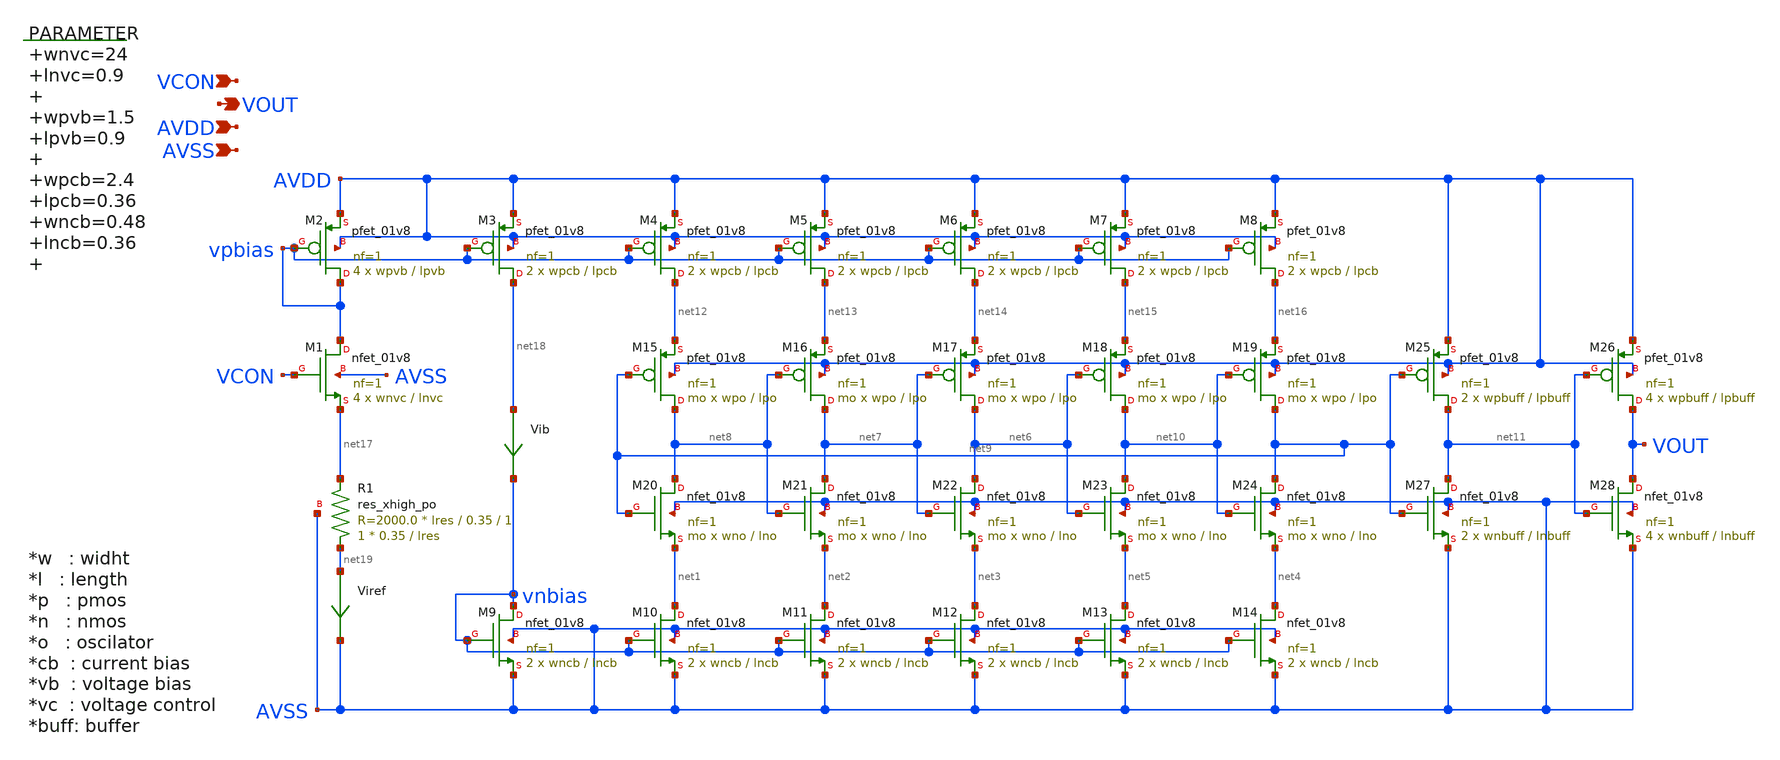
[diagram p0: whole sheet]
** sch_path: xschem/vco.sch
**.subckt vco VCON VOUT AVDD AVSS
*.ipin VCON
*.opin VOUT
*.ipin AVDD
*.ipin AVSS
.param wnvc=24 lnvc=0.9 wpvb=1.5 lpvb=0.9 wpcb=2.4 lpcb=0.36 wncb=0.48 lncb=0.36 wpo=2 lpo=0.54
+ wno=1 lno=0.54 mo=2 wpbuff=2.4 lpbuff=0.18 wnbuff=0.6 lnbuff=0.18 lres=5.25

XR1 net19 net17 AVSS sky130_fd_pr__res_xhigh_po W=0.35 L=lres mult=1 m=1
XM1 vpbias VCON net17 AVSS sky130_fd_pr__nfet_01v8 L=lnvc W=wnvc nf=1 ad='int((nf+1)/2) * W/nf * 0.29'
+ as='int((nf+2)/2) * W/nf * 0.29' pd='2*int((nf+1)/2) * (W/nf + 0.29)' ps='2*int((nf+2)/2) * (W/nf + 0.29)'
+ nrd='0.29 / W' nrs='0.29 / W' sa=0 sb=0 sd=0 mult=4 m=4
XM2 vpbias vpbias AVDD AVDD sky130_fd_pr__pfet_01v8 L=lpvb W=wpvb nf=1 ad='int((nf+1)/2) * W/nf * 0.29'
+ as='int((nf+2)/2) * W/nf * 0.29' pd='2*int((nf+1)/2) * (W/nf + 0.29)' ps='2*int((nf+2)/2) * (W/nf + 0.29)'
+ nrd='0.29 / W' nrs='0.29 / W' sa=0 sb=0 sd=0 mult=4 m=4
XM3 net18 vpbias AVDD AVDD sky130_fd_pr__pfet_01v8 L=lpcb W=wpcb nf=1 ad='int((nf+1)/2) * W/nf * 0.29'
+ as='int((nf+2)/2) * W/nf * 0.29' pd='2*int((nf+1)/2) * (W/nf + 0.29)' ps='2*int((nf+2)/2) * (W/nf + 0.29)'
+ nrd='0.29 / W' nrs='0.29 / W' sa=0 sb=0 sd=0 mult=2 m=2
XM4 net12 vpbias AVDD AVDD sky130_fd_pr__pfet_01v8 L=lpcb W=wpcb nf=1 ad='int((nf+1)/2) * W/nf * 0.29'
+ as='int((nf+2)/2) * W/nf * 0.29' pd='2*int((nf+1)/2) * (W/nf + 0.29)' ps='2*int((nf+2)/2) * (W/nf + 0.29)'
+ nrd='0.29 / W' nrs='0.29 / W' sa=0 sb=0 sd=0 mult=2 m=2
XM5 net13 vpbias AVDD AVDD sky130_fd_pr__pfet_01v8 L=lpcb W=wpcb nf=1 ad='int((nf+1)/2) * W/nf * 0.29'
+ as='int((nf+2)/2) * W/nf * 0.29' pd='2*int((nf+1)/2) * (W/nf + 0.29)' ps='2*int((nf+2)/2) * (W/nf + 0.29)'
+ nrd='0.29 / W' nrs='0.29 / W' sa=0 sb=0 sd=0 mult=2 m=2
XM6 net14 vpbias AVDD AVDD sky130_fd_pr__pfet_01v8 L=lpcb W=wpcb nf=1 ad='int((nf+1)/2) * W/nf * 0.29'
+ as='int((nf+2)/2) * W/nf * 0.29' pd='2*int((nf+1)/2) * (W/nf + 0.29)' ps='2*int((nf+2)/2) * (W/nf + 0.29)'
+ nrd='0.29 / W' nrs='0.29 / W' sa=0 sb=0 sd=0 mult=2 m=2
XM7 net15 vpbias AVDD AVDD sky130_fd_pr__pfet_01v8 L=lpcb W=wpcb nf=1 ad='int((nf+1)/2) * W/nf * 0.29'
+ as='int((nf+2)/2) * W/nf * 0.29' pd='2*int((nf+1)/2) * (W/nf + 0.29)' ps='2*int((nf+2)/2) * (W/nf + 0.29)'
+ nrd='0.29 / W' nrs='0.29 / W' sa=0 sb=0 sd=0 mult=2 m=2
XM8 net16 vpbias AVDD AVDD sky130_fd_pr__pfet_01v8 L=lpcb W=wpcb nf=1 ad='int((nf+1)/2) * W/nf * 0.29'
+ as='int((nf+2)/2) * W/nf * 0.29' pd='2*int((nf+1)/2) * (W/nf + 0.29)' ps='2*int((nf+2)/2) * (W/nf + 0.29)'
+ nrd='0.29 / W' nrs='0.29 / W' sa=0 sb=0 sd=0 mult=2 m=2
XM9 vnbias vnbias AVSS AVSS sky130_fd_pr__nfet_01v8 L=lncb W=wncb nf=1 ad='int((nf+1)/2) * W/nf * 0.29'
+ as='int((nf+2)/2) * W/nf * 0.29' pd='2*int((nf+1)/2) * (W/nf + 0.29)' ps='2*int((nf+2)/2) * (W/nf + 0.29)'
+ nrd='0.29 / W' nrs='0.29 / W' sa=0 sb=0 sd=0 mult=2 m=2
XM10 net1 vnbias AVSS AVSS sky130_fd_pr__nfet_01v8 L=lncb W=wncb nf=1 ad='int((nf+1)/2) * W/nf * 0.29'
+ as='int((nf+2)/2) * W/nf * 0.29' pd='2*int((nf+1)/2) * (W/nf + 0.29)' ps='2*int((nf+2)/2) * (W/nf + 0.29)'
+ nrd='0.29 / W' nrs='0.29 / W' sa=0 sb=0 sd=0 mult=2 m=2
XM11 net2 vnbias AVSS AVSS sky130_fd_pr__nfet_01v8 L=lncb W=wncb nf=1 ad='int((nf+1)/2) * W/nf * 0.29'
+ as='int((nf+2)/2) * W/nf * 0.29' pd='2*int((nf+1)/2) * (W/nf + 0.29)' ps='2*int((nf+2)/2) * (W/nf + 0.29)'
+ nrd='0.29 / W' nrs='0.29 / W' sa=0 sb=0 sd=0 mult=2 m=2
XM12 net3 vnbias AVSS AVSS sky130_fd_pr__nfet_01v8 L=lncb W=wncb nf=1 ad='int((nf+1)/2) * W/nf * 0.29'
+ as='int((nf+2)/2) * W/nf * 0.29' pd='2*int((nf+1)/2) * (W/nf + 0.29)' ps='2*int((nf+2)/2) * (W/nf + 0.29)'
+ nrd='0.29 / W' nrs='0.29 / W' sa=0 sb=0 sd=0 mult=2 m=2
XM13 net5 vnbias AVSS AVSS sky130_fd_pr__nfet_01v8 L=lncb W=wncb nf=1 ad='int((nf+1)/2) * W/nf * 0.29'
+ as='int((nf+2)/2) * W/nf * 0.29' pd='2*int((nf+1)/2) * (W/nf + 0.29)' ps='2*int((nf+2)/2) * (W/nf + 0.29)'
+ nrd='0.29 / W' nrs='0.29 / W' sa=0 sb=0 sd=0 mult=2 m=2
XM14 net4 vnbias AVSS AVSS sky130_fd_pr__nfet_01v8 L=lncb W=wncb nf=1 ad='int((nf+1)/2) * W/nf * 0.29'
+ as='int((nf+2)/2) * W/nf * 0.29' pd='2*int((nf+1)/2) * (W/nf + 0.29)' ps='2*int((nf+2)/2) * (W/nf + 0.29)'
+ nrd='0.29 / W' nrs='0.29 / W' sa=0 sb=0 sd=0 mult=2 m=2
XM15 net8 net9 net12 AVDD sky130_fd_pr__pfet_01v8 L=lpo W=wpo nf=1 ad='int((nf+1)/2) * W/nf * 0.29' as='int((nf+2)/2) * W/nf * 0.29'
+ pd='2*int((nf+1)/2) * (W/nf + 0.29)' ps='2*int((nf+2)/2) * (W/nf + 0.29)' nrd='0.29 / W' nrs='0.29 / W'
+ sa=0 sb=0 sd=0 mult=mo m=mo
XM16 net7 net8 net13 AVDD sky130_fd_pr__pfet_01v8 L=lpo W=wpo nf=1 ad='int((nf+1)/2) * W/nf * 0.29' as='int((nf+2)/2) * W/nf * 0.29'
+ pd='2*int((nf+1)/2) * (W/nf + 0.29)' ps='2*int((nf+2)/2) * (W/nf + 0.29)' nrd='0.29 / W' nrs='0.29 / W'
+ sa=0 sb=0 sd=0 mult=mo m=mo
XM17 net6 net7 net14 AVDD sky130_fd_pr__pfet_01v8 L=lpo W=wpo nf=1 ad='int((nf+1)/2) * W/nf * 0.29' as='int((nf+2)/2) * W/nf * 0.29'
+ pd='2*int((nf+1)/2) * (W/nf + 0.29)' ps='2*int((nf+2)/2) * (W/nf + 0.29)' nrd='0.29 / W' nrs='0.29 / W'
+ sa=0 sb=0 sd=0 mult=mo m=mo
XM18 net10 net6 net15 AVDD sky130_fd_pr__pfet_01v8 L=lpo W=wpo nf=1 ad='int((nf+1)/2) * W/nf * 0.29'
+ as='int((nf+2)/2) * W/nf * 0.29' pd='2*int((nf+1)/2) * (W/nf + 0.29)' ps='2*int((nf+2)/2) * (W/nf + 0.29)'
+ nrd='0.29 / W' nrs='0.29 / W' sa=0 sb=0 sd=0 mult=mo m=mo
XM19 net9 net10 net16 AVDD sky130_fd_pr__pfet_01v8 L=lpo W=wpo nf=1 ad='int((nf+1)/2) * W/nf * 0.29'
+ as='int((nf+2)/2) * W/nf * 0.29' pd='2*int((nf+1)/2) * (W/nf + 0.29)' ps='2*int((nf+2)/2) * (W/nf + 0.29)'
+ nrd='0.29 / W' nrs='0.29 / W' sa=0 sb=0 sd=0 mult=mo m=mo
XM20 net8 net9 net1 AVSS sky130_fd_pr__nfet_01v8 L=lno W=wno nf=1 ad='int((nf+1)/2) * W/nf * 0.29' as='int((nf+2)/2) * W/nf * 0.29'
+ pd='2*int((nf+1)/2) * (W/nf + 0.29)' ps='2*int((nf+2)/2) * (W/nf + 0.29)' nrd='0.29 / W' nrs='0.29 / W'
+ sa=0 sb=0 sd=0 mult=mo m=mo
XM21 net7 net8 net2 AVSS sky130_fd_pr__nfet_01v8 L=lno W=wno nf=1 ad='int((nf+1)/2) * W/nf * 0.29' as='int((nf+2)/2) * W/nf * 0.29'
+ pd='2*int((nf+1)/2) * (W/nf + 0.29)' ps='2*int((nf+2)/2) * (W/nf + 0.29)' nrd='0.29 / W' nrs='0.29 / W'
+ sa=0 sb=0 sd=0 mult=mo m=mo
XM22 net6 net7 net3 AVSS sky130_fd_pr__nfet_01v8 L=lno W=wno nf=1 ad='int((nf+1)/2) * W/nf * 0.29' as='int((nf+2)/2) * W/nf * 0.29'
+ pd='2*int((nf+1)/2) * (W/nf + 0.29)' ps='2*int((nf+2)/2) * (W/nf + 0.29)' nrd='0.29 / W' nrs='0.29 / W'
+ sa=0 sb=0 sd=0 mult=mo m=mo
XM23 net10 net6 net5 AVSS sky130_fd_pr__nfet_01v8 L=lno W=wno nf=1 ad='int((nf+1)/2) * W/nf * 0.29' as='int((nf+2)/2) * W/nf * 0.29'
+ pd='2*int((nf+1)/2) * (W/nf + 0.29)' ps='2*int((nf+2)/2) * (W/nf + 0.29)' nrd='0.29 / W' nrs='0.29 / W'
+ sa=0 sb=0 sd=0 mult=mo m=mo
XM24 net9 net10 net4 AVSS sky130_fd_pr__nfet_01v8 L=lno W=wno nf=1 ad='int((nf+1)/2) * W/nf * 0.29' as='int((nf+2)/2) * W/nf * 0.29'
+ pd='2*int((nf+1)/2) * (W/nf + 0.29)' ps='2*int((nf+2)/2) * (W/nf + 0.29)' nrd='0.29 / W' nrs='0.29 / W'
+ sa=0 sb=0 sd=0 mult=mo m=mo
XM25 net11 net9 AVDD AVDD sky130_fd_pr__pfet_01v8 L=lpbuff W=wpbuff nf=1 ad='int((nf+1)/2) * W/nf * 0.29'
+ as='int((nf+2)/2) * W/nf * 0.29' pd='2*int((nf+1)/2) * (W/nf + 0.29)' ps='2*int((nf+2)/2) * (W/nf + 0.29)'
+ nrd='0.29 / W' nrs='0.29 / W' sa=0 sb=0 sd=0 mult=2 m=2
XM26 VOUT net11 AVDD AVDD sky130_fd_pr__pfet_01v8 L=lpbuff W=wpbuff nf=1 ad='int((nf+1)/2) * W/nf * 0.29'
+ as='int((nf+2)/2) * W/nf * 0.29' pd='2*int((nf+1)/2) * (W/nf + 0.29)' ps='2*int((nf+2)/2) * (W/nf + 0.29)'
+ nrd='0.29 / W' nrs='0.29 / W' sa=0 sb=0 sd=0 mult=4 m=4
XM27 net11 net9 AVSS AVSS sky130_fd_pr__nfet_01v8 L=lnbuff W=wnbuff nf=1 ad='int((nf+1)/2) * W/nf * 0.29'
+ as='int((nf+2)/2) * W/nf * 0.29' pd='2*int((nf+1)/2) * (W/nf + 0.29)' ps='2*int((nf+2)/2) * (W/nf + 0.29)'
+ nrd='0.29 / W' nrs='0.29 / W' sa=0 sb=0 sd=0 mult=2 m=2
XM28 VOUT net11 AVSS AVSS sky130_fd_pr__nfet_01v8 L=lnbuff W=wnbuff nf=1 ad='int((nf+1)/2) * W/nf * 0.29'
+ as='int((nf+2)/2) * W/nf * 0.29' pd='2*int((nf+1)/2) * (W/nf + 0.29)' ps='2*int((nf+2)/2) * (W/nf + 0.29)'
+ nrd='0.29 / W' nrs='0.29 / W' sa=0 sb=0 sd=0 mult=4 m=4
Viref net19 AVSS 0
.save i(viref)
Vib net18 vnbias 0
.save i(vib)
**.ends
.end
